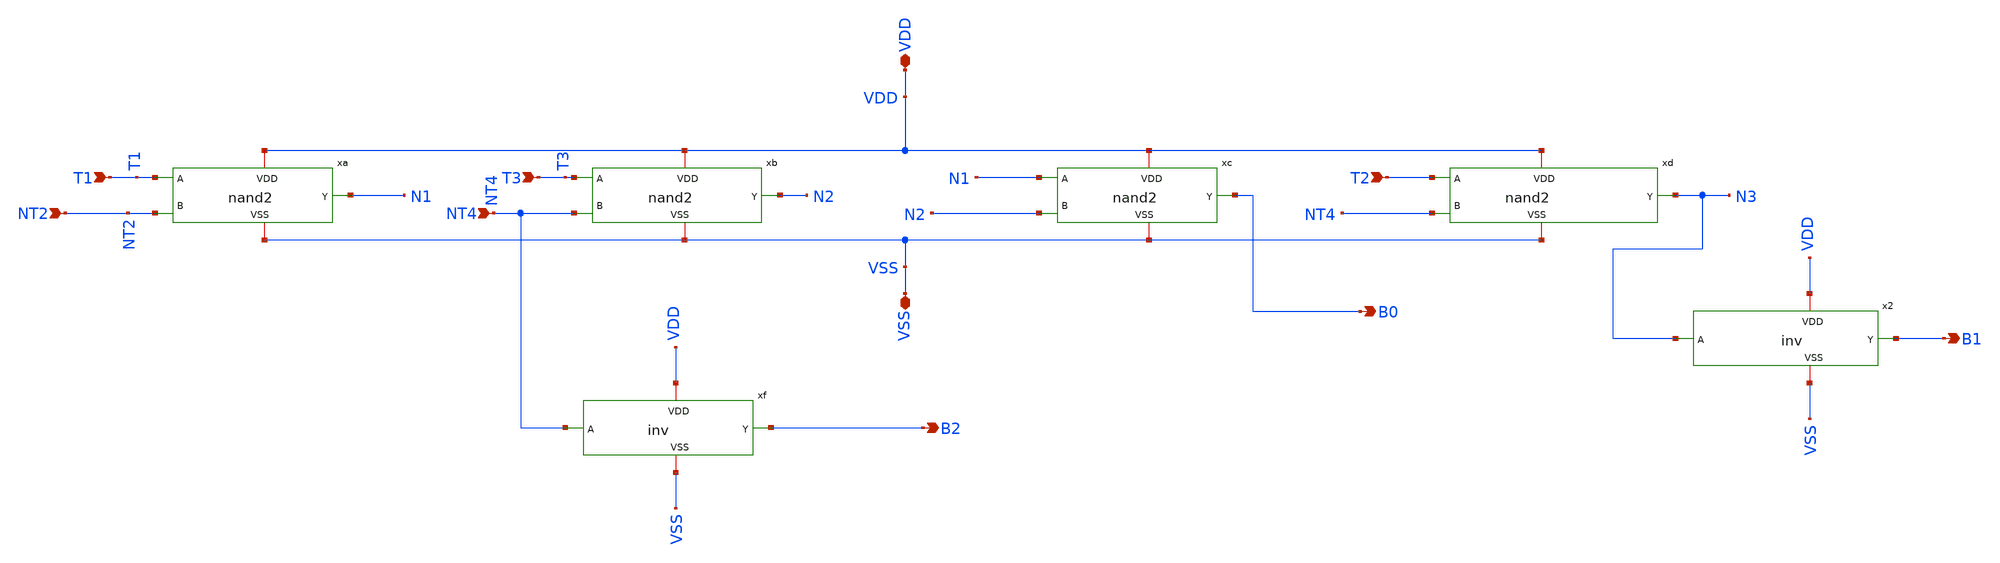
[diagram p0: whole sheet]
** sch_path: schematics/therm_to_bin.sch
**.subckt therm_to_bin T1 NT2 T3 NT4 B0 T2 VDD VSS B2 B1
*.ipin T1
*.ipin NT2
*.ipin T3
*.ipin NT4
*.opin B0
*.ipin T2
*.iopin VDD
*.iopin VSS
*.opin B2
*.opin B1
xa VDD T1 N1 NT2 VSS nand2
xb VDD T3 N2 NT4 VSS nand2
xc VDD N1 B0 N2 VSS nand2
xd VDD T2 N3 NT4 VSS nand2
xf VDD NT4 B2 VSS inv
x2 VDD N3 B1 VSS inv
**.ends
.end
